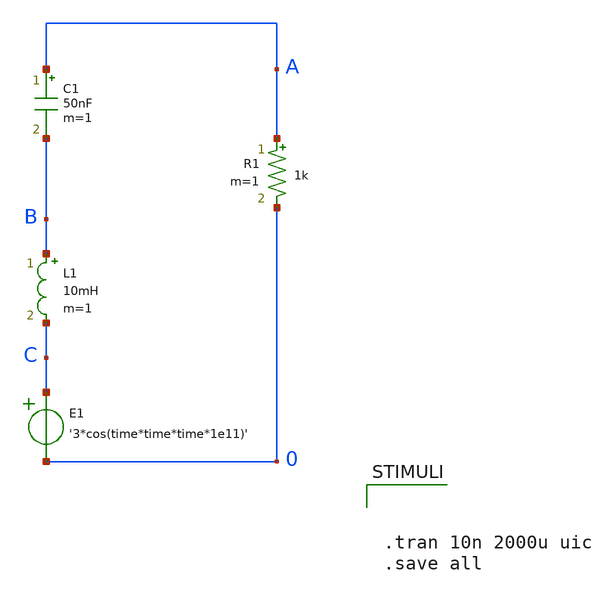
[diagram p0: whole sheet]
** sch_path: xschem_library/examples/rlc.sch
**.subckt rlc
C1 A B 50nF m=1
E1 C 0 VOL=' '3*cos(time*time*time*1e11)' '
R1 A 0 1k m=1
L1 B C 10mH m=1
**** begin user architecture code



.tran 10n 2000u uic
.save all


**** end user architecture code
**.ends
.end
